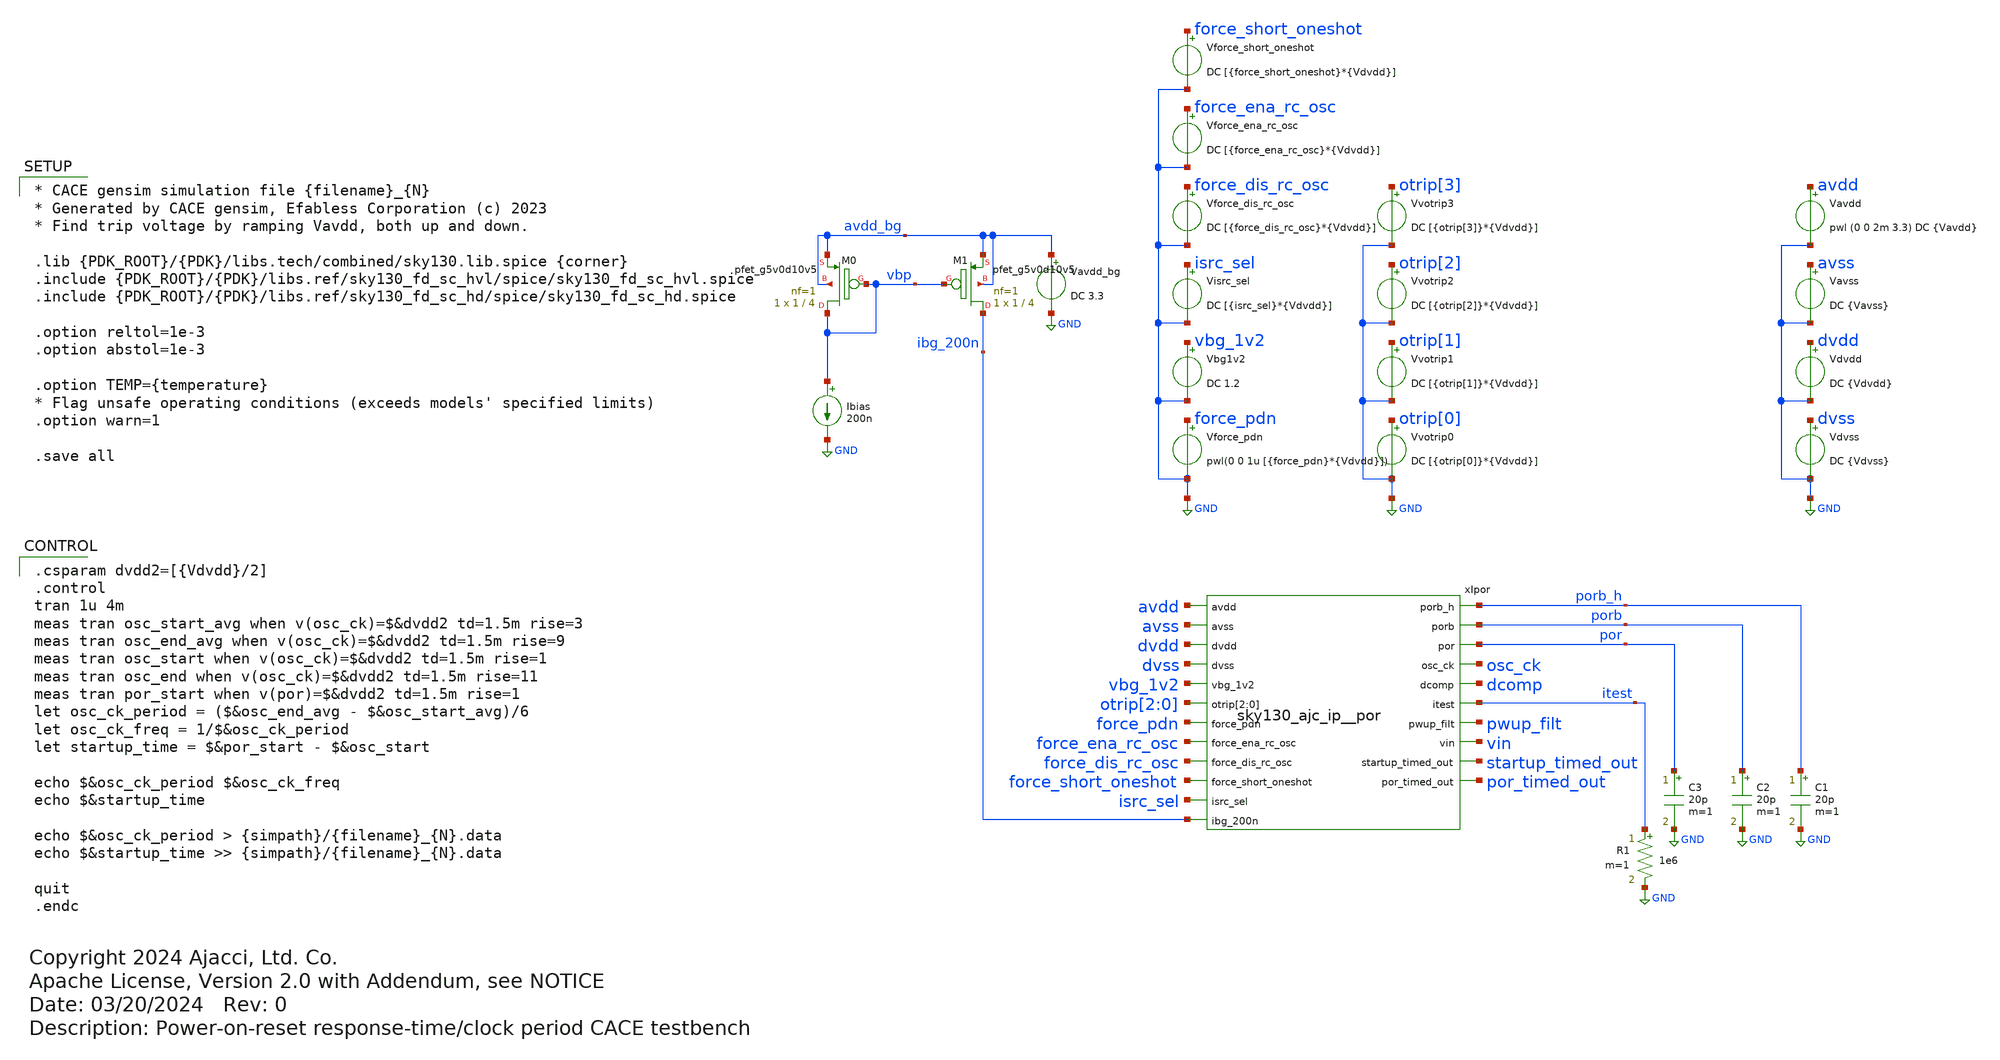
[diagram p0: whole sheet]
** sch_path: cace/response_time.sch
* Copyright 2024 Ajacci, Ltd. Co.
* Apache License, Version 2.0 with Addendum, see NOTICE
**.subckt response_time
Ibias vbp GND 200n
XM1 ibg_200n vbp avdd_bg avdd_bg sky130_fd_pr__pfet_g5v0d10v5 L=4 W=1 nf=1 ad='int((nf+1)/2) * W/nf * 0.29'
+ as='int((nf+2)/2) * W/nf * 0.29' pd='2*int((nf+1)/2) * (W/nf + 0.29)' ps='2*int((nf+2)/2) * (W/nf + 0.29)'
+ nrd='0.29 / W' nrs='0.29 / W' sa=0 sb=0 sd=0 mult=1 m=1
XM0 vbp vbp avdd_bg avdd_bg sky130_fd_pr__pfet_g5v0d10v5 L=4 W=1 nf=1 ad='int((nf+1)/2) * W/nf * 0.29'
+ as='int((nf+2)/2) * W/nf * 0.29' pd='2*int((nf+1)/2) * (W/nf + 0.29)' ps='2*int((nf+2)/2) * (W/nf + 0.29)'
+ nrd='0.29 / W' nrs='0.29 / W' sa=0 sb=0 sd=0 mult=1 m=1
R1 itest GND 1e6 m=1
Vavss avss GND DC {Vavss}
Vforce_pdn force_pdn GND pwl(0 0 1u [{force_pdn}*{Vdvdd}])
Vavdd avdd GND pwl (0 0 2m 3.3) DC {Vavdd}
.save i(vavdd)
Vbg1v2 vbg_1v2 GND DC 1.2
Vdvss dvss GND DC {Vdvss}
Vdvdd dvdd GND DC {Vdvdd}
.save i(vdvdd)
Vvotrip0 otrip[0] GND DC [{otrip[0]}*{Vdvdd}]
.save i(vvotrip0)
Vvotrip1 otrip[1] GND DC [{otrip[1]}*{Vdvdd}]
.save i(vvotrip1)
Vvotrip2 otrip[2] GND DC [{otrip[2]}*{Vdvdd}]
.save i(vvotrip2)
Vvotrip3 otrip[3] GND DC [{otrip[3]}*{Vdvdd}]
.save i(vvotrip3)
Visrc_sel isrc_sel GND DC [{isrc_sel}*{Vdvdd}]
Vavdd_bg avdd_bg GND DC 3.3
Vforce_dis_rc_osc force_dis_rc_osc GND DC [{force_dis_rc_osc}*{Vdvdd}]
Vforce_short_oneshot force_short_oneshot GND DC [{force_short_oneshot}*{Vdvdd}]
Vforce_ena_rc_osc force_ena_rc_osc GND DC [{force_ena_rc_osc}*{Vdvdd}]
xIpor avdd porb_h porb avss dvdd por dvss osc_ck vbg_1v2 dcomp otrip[2] otrip[1] otrip[0] itest
+ force_pdn pwup_filt vin force_ena_rc_osc force_dis_rc_osc startup_timed_out por_timed_out force_short_oneshot
+ isrc_sel ibg_200n sky130_ajc_ip__por
C1 porb_h GND 20p m=1
C2 porb GND 20p m=1
C3 por GND 20p m=1
**** begin user architecture code

* CACE gensim simulation file {filename}_{N}
* Generated by CACE gensim, Efabless Corporation (c) 2023
* Find trip voltage by ramping Vavdd, both up and down.

.lib {PDK_ROOT}/{PDK}/libs.tech/combined/sky130.lib.spice {corner}
.include {PDK_ROOT}/{PDK}/libs.ref/sky130_fd_sc_hvl/spice/sky130_fd_sc_hvl.spice
.include {PDK_ROOT}/{PDK}/libs.ref/sky130_fd_sc_hd/spice/sky130_fd_sc_hd.spice

.option reltol=1e-3
.option abstol=1e-3

.option TEMP={temperature}
* Flag unsafe operating conditions (exceeds models' specified limits)
.option warn=1

.save all



.csparam dvdd2=[{Vdvdd}/2]
.control
tran 1u 4m
meas tran osc_start_avg when v(osc_ck)=$&dvdd2 td=1.5m rise=3
meas tran osc_end_avg when v(osc_ck)=$&dvdd2 td=1.5m rise=9
meas tran osc_start when v(osc_ck)=$&dvdd2 td=1.5m rise=1
meas tran osc_end when v(osc_ck)=$&dvdd2 td=1.5m rise=11
meas tran por_start when v(por)=$&dvdd2 td=1.5m rise=1
let osc_ck_period = ($&osc_end_avg - $&osc_start_avg)/6
let osc_ck_freq = 1/$&osc_ck_period
let startup_time = $&por_start - $&osc_start

echo $&osc_ck_period $&osc_ck_freq
echo $&startup_time

echo $&osc_ck_period > {simpath}/{filename}_{N}.data
echo $&startup_time >> {simpath}/{filename}_{N}.data

quit
.endc


**** end user architecture code
**.ends
.GLOBAL GND
.end
